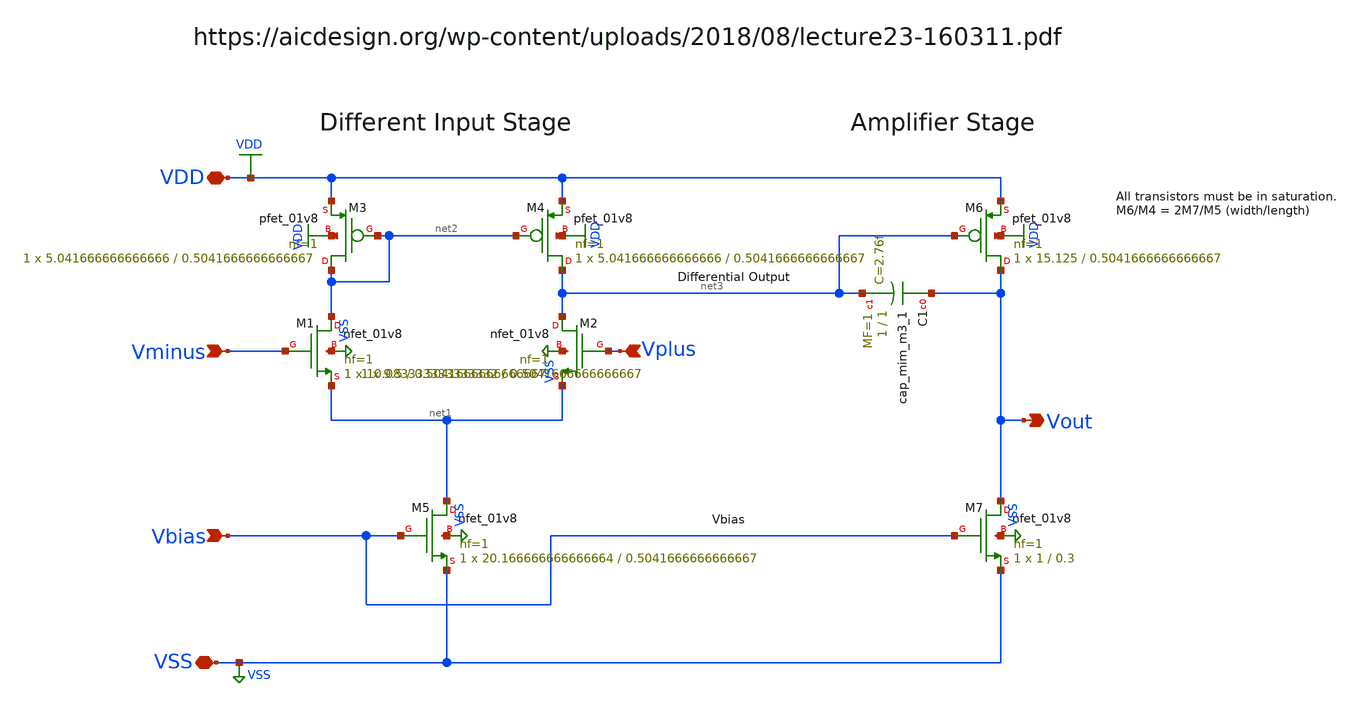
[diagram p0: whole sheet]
** sch_path: examples/template/temp_schemsym_ba97f9655c8a4c628645f348d918d925.sch
**.subckt temp_schemsym_ba97f9655c8a4c628645f348d918d925 Vplus Vminus VDD VSS Vbias Vout
*.ipin Vplus
*.ipin Vminus
*.iopin VDD
*.iopin VSS
*.ipin Vbias
*.opin Vout
XM1 net2 Vminus net1 VSS sky130_fd_pr__nfet_01v8 L=0.5041666666666667 W=10.083333333333332 nf=1 ad='int((nf+1)/2) * W/nf * 0.29'
+ as='int((nf+2)/2) * W/nf * 0.29' pd='2*int((nf+1)/2) * (W/nf + 0.29)' ps='2*int((nf+2)/2) * (W/nf + 0.29)'
+ nrd='0.29 / W' nrs='0.29 / W' sa=0 sb=0 sd=0 mult=1 m=1
XM2 net3 Vplus net1 VSS sky130_fd_pr__nfet_01v8 L=0.5041666666666667 W=9.5 nf=1 ad='int((nf+1)/2) * W/nf * 0.29'
+ as='int((nf+2)/2) * W/nf * 0.29' pd='2*int((nf+1)/2) * (W/nf + 0.29)' ps='2*int((nf+2)/2) * (W/nf + 0.29)'
+ nrd='0.29 / W' nrs='0.29 / W' sa=0 sb=0 sd=0 mult=1 m=1
XM3 net2 net2 VDD VDD sky130_fd_pr__pfet_01v8 L=0.5041666666666667 W=5.041666666666666 nf=1 ad='int((nf+1)/2) * W/nf * 0.29'
+ as='int((nf+2)/2) * W/nf * 0.29' pd='2*int((nf+1)/2) * (W/nf + 0.29)' ps='2*int((nf+2)/2) * (W/nf + 0.29)'
+ nrd='0.29 / W' nrs='0.29 / W' sa=0 sb=0 sd=0 mult=1 m=1
XM4 net3 net2 VDD VDD sky130_fd_pr__pfet_01v8 L=0.5041666666666667 W=5.041666666666666 nf=1 ad='int((nf+1)/2) * W/nf * 0.29'
+ as='int((nf+2)/2) * W/nf * 0.29' pd='2*int((nf+1)/2) * (W/nf + 0.29)' ps='2*int((nf+2)/2) * (W/nf + 0.29)'
+ nrd='0.29 / W' nrs='0.29 / W' sa=0 sb=0 sd=0 mult=1 m=1
XM5 net1 Vbias VSS VSS sky130_fd_pr__nfet_01v8 L=0.5041666666666667 W=20.166666666666664 nf=1 ad='int((nf+1)/2) * W/nf * 0.29'
+ as='int((nf+2)/2) * W/nf * 0.29' pd='2*int((nf+1)/2) * (W/nf + 0.29)' ps='2*int((nf+2)/2) * (W/nf + 0.29)'
+ nrd='0.29 / W' nrs='0.29 / W' sa=0 sb=0 sd=0 mult=1 m=1
XM6 Vout net3 VDD VDD sky130_fd_pr__pfet_01v8 L=0.5041666666666667 W=15.125 nf=1 ad='int((nf+1)/2) * W/nf * 0.29'
+ as='int((nf+2)/2) * W/nf * 0.29' pd='2*int((nf+1)/2) * (W/nf + 0.29)' ps='2*int((nf+2)/2) * (W/nf + 0.29)'
+ nrd='0.29 / W' nrs='0.29 / W' sa=0 sb=0 sd=0 mult=1 m=1
XC1 Vout net3 sky130_fd_pr__cap_mim_m3_1 W=1 L=1 MF=1 m=1
XM7 Vout Vbias VSS VSS sky130_fd_pr__nfet_01v8 L=0.3 W=1 nf=1 ad='int((nf+1)/2) * W/nf * 0.29' as='int((nf+2)/2) * W/nf * 0.29'
+ pd='2*int((nf+1)/2) * (W/nf + 0.29)' ps='2*int((nf+2)/2) * (W/nf + 0.29)' nrd='0.29 / W' nrs='0.29 / W'
+ sa=0 sb=0 sd=0 mult=1 m=1
**.ends
.GLOBAL VDD
.GLOBAL VSS
.end
